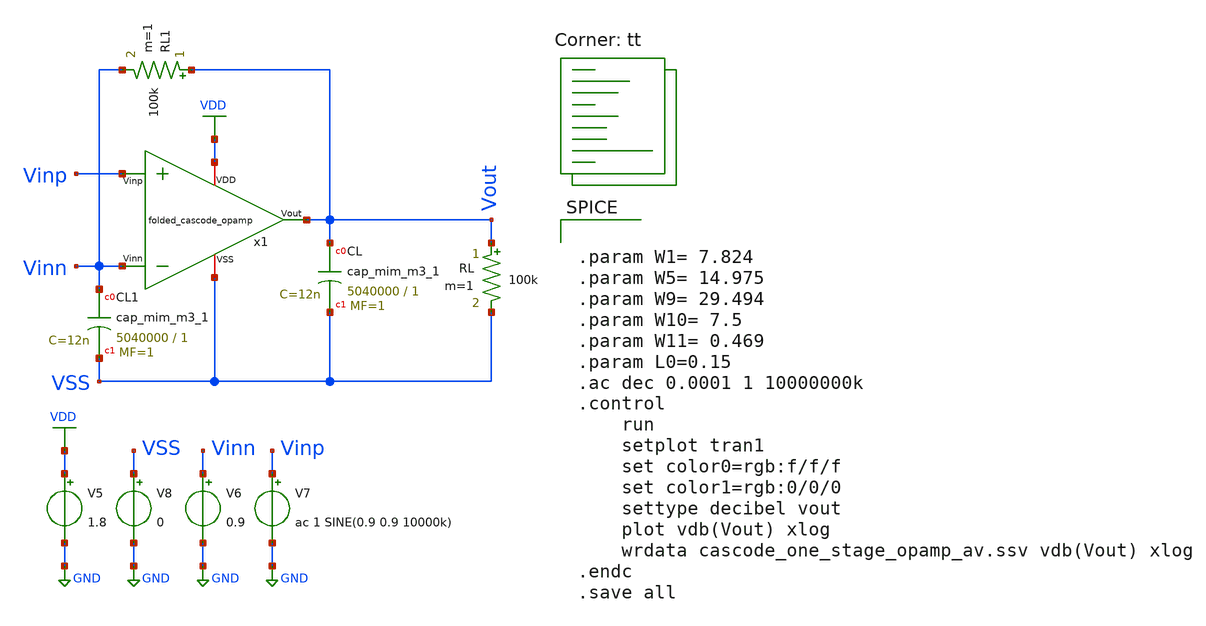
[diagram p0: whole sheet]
** sch_path: opamp_design/folded_cascode_opamp/folded_one_stage_opamp_av.sch
**.subckt folded_one_stage_opamp_av
XCL Vout VSS sky130_fd_pr__cap_mim_m3_1 W=5040000 L=1 MF=1 m=1
RL Vout VSS 100k m=1
XCL1 Vinn VSS sky130_fd_pr__cap_mim_m3_1 W=5040000 L=1 MF=1 m=1
RL1 Vout Vinn 100k m=1
V5 VDD GND 1.8
V6 Vinn GND 0.9
V7 Vinp GND ac 1 SINE(0.9 0.9 10000k)
V8 VSS GND 0
x1 VDD Vout Vinp Vinn VSS folded_cascode_opamp
**** begin user architecture code
.lib $::SKYWATER_MODELS/sky130.lib.spice tt


.param W1= 7.824
.param W5= 14.975
.param W9= 29.494
.param W10= 7.5
.param W11= 0.469
.param L0=0.15
.ac dec 0.0001 1 10000000k
.control
	run
	setplot tran1
	set color0=rgb:f/f/f
	set color1=rgb:0/0/0
	settype decibel vout
	plot vdb(Vout) xlog
	wrdata cascode_one_stage_opamp_av.ssv vdb(Vout) xlog
.endc
.save all


**** end user architecture code
**.ends

* expanding   symbol:
*+  /home/ricardo/RATT_repos/Proyectos_xschem/opamp_design/folded_cascode_opamp/folded_cascode_opamp.sym # of pins=5
** sym_path: opamp_design/folded_cascode_opamp/folded_cascode_opamp.sym
** sch_path: opamp_design/folded_cascode_opamp/folded_cascode_opamp.sch
.subckt folded_cascode_opamp VDD Vout Vinp Vinn VSS
*.opin Vout
*.ipin Vinn
*.ipin Vinp
*.iopin VDD
*.iopin VSS
XM11 net4 net2 VSS VSS sky130_fd_pr__nfet_01v8 L={L0} W={W8} nf=1 ad='int((nf+1)/2) * W/nf * 0.29' as='int((nf+2)/2) * W/nf * 0.29'
+ pd='2*int((nf+1)/2) * (W/nf + 0.29)' ps='2*int((nf+2)/2) * (W/nf + 0.29)' nrd='0.29 / W' nrs='0.29 / W'
+ sa=0 sb=0 sd=0 mult=1 m=1
XM10 net3 net2 VSS VSS sky130_fd_pr__nfet_01v8 L={L0} W={W8} nf=1 ad='int((nf+1)/2) * W/nf * 0.29' as='int((nf+2)/2) * W/nf * 0.29'
+ pd='2*int((nf+1)/2) * (W/nf + 0.29)' ps='2*int((nf+2)/2) * (W/nf + 0.29)' nrd='0.29 / W' nrs='0.29 / W'
+ sa=0 sb=0 sd=0 mult=1 m=1
XM8 net2 net1 net3 VSS sky130_fd_pr__nfet_01v8 L={L0} W={W8} nf=1 ad='int((nf+1)/2) * W/nf * 0.29' as='int((nf+2)/2) * W/nf * 0.29'
+ pd='2*int((nf+1)/2) * (W/nf + 0.29)' ps='2*int((nf+2)/2) * (W/nf + 0.29)' nrd='0.29 / W' nrs='0.29 / W'
+ sa=0 sb=0 sd=0 mult=1 m=1
XM9 Vout net1 net4 VSS sky130_fd_pr__nfet_01v8 L={L0} W={W8} nf=1 ad='int((nf+1)/2) * W/nf * 0.29' as='int((nf+2)/2) * W/nf * 0.29'
+ pd='2*int((nf+1)/2) * (W/nf + 0.29)' ps='2*int((nf+2)/2) * (W/nf + 0.29)' nrd='0.29 / W' nrs='0.29 / W'
+ sa=0 sb=0 sd=0 mult=1 m=1
XM7 Vout net5 net8 VDD sky130_fd_pr__pfet_01v8 L={L0} W={W6} nf=1 ad='int((nf+1)/2) * W/nf * 0.29' as='int((nf+2)/2) * W/nf * 0.29'
+ pd='2*int((nf+1)/2) * (W/nf + 0.29)' ps='2*int((nf+2)/2) * (W/nf + 0.29)' nrd='0.29 / W' nrs='0.29 / W'
+ sa=0 sb=0 sd=0 mult=1 m=1
XM6 net2 net5 net7 VDD sky130_fd_pr__pfet_01v8 L={L0} W={W6} nf=1 ad='int((nf+1)/2) * W/nf * 0.29' as='int((nf+2)/2) * W/nf * 0.29'
+ pd='2*int((nf+1)/2) * (W/nf + 0.29)' ps='2*int((nf+2)/2) * (W/nf + 0.29)' nrd='0.29 / W' nrs='0.29 / W'
+ sa=0 sb=0 sd=0 mult=1 m=1
XM1 net7 Vinp net6 VSS sky130_fd_pr__nfet_01v8 L={L0} W={W1} nf=1 ad='int((nf+1)/2) * W/nf * 0.29' as='int((nf+2)/2) * W/nf * 0.29'
+ pd='2*int((nf+1)/2) * (W/nf + 0.29)' ps='2*int((nf+2)/2) * (W/nf + 0.29)' nrd='0.29 / W' nrs='0.29 / W'
+ sa=0 sb=0 sd=0 mult=1 m=1
XM2 net8 Vinn net6 VSS sky130_fd_pr__nfet_01v8 L={L0} W={W1} nf=1 ad='int((nf+1)/2) * W/nf * 0.29' as='int((nf+2)/2) * W/nf * 0.29'
+ pd='2*int((nf+1)/2) * (W/nf + 0.29)' ps='2*int((nf+2)/2) * (W/nf + 0.29)' nrd='0.29 / W' nrs='0.29 / W'
+ sa=0 sb=0 sd=0 mult=1 m=1
XM3 net6 net10 VSS VSS sky130_fd_pr__nfet_01v8 L={L0} W={W3} nf=1 ad='int((nf+1)/2) * W/nf * 0.29' as='int((nf+2)/2) * W/nf * 0.29'
+ pd='2*int((nf+1)/2) * (W/nf + 0.29)' ps='2*int((nf+2)/2) * (W/nf + 0.29)' nrd='0.29 / W' nrs='0.29 / W'
+ sa=0 sb=0 sd=0 mult=1 m=1
XM4 net7 net9 VDD VDD sky130_fd_pr__pfet_01v8 L={L0} W={W4} nf=1 ad='int((nf+1)/2) * W/nf * 0.29' as='int((nf+2)/2) * W/nf * 0.29'
+ pd='2*int((nf+1)/2) * (W/nf + 0.29)' ps='2*int((nf+2)/2) * (W/nf + 0.29)' nrd='0.29 / W' nrs='0.29 / W'
+ sa=0 sb=0 sd=0 mult=1 m=1
XM5 net8 net9 VDD VDD sky130_fd_pr__pfet_01v8 L={L0} W={W4} nf=1 ad='int((nf+1)/2) * W/nf * 0.29' as='int((nf+2)/2) * W/nf * 0.29'
+ pd='2*int((nf+1)/2) * (W/nf + 0.29)' ps='2*int((nf+2)/2) * (W/nf + 0.29)' nrd='0.29 / W' nrs='0.29 / W'
+ sa=0 sb=0 sd=0 mult=1 m=1
XC1 Vout VSS sky130_fd_pr__cap_mim_m3_1 W=1 L=1 MF=1 m=1
XM12 net9 net9 VDD VDD sky130_fd_pr__pfet_01v8 L={L0} W={W4} nf=1 ad='int((nf+1)/2) * W/nf * 0.29' as='int((nf+2)/2) * W/nf * 0.29'
+ pd='2*int((nf+1)/2) * (W/nf + 0.29)' ps='2*int((nf+2)/2) * (W/nf + 0.29)' nrd='0.29 / W' nrs='0.29 / W'
+ sa=0 sb=0 sd=0 mult=1 m=1
I4 net9 VSS 10u
XM13 net5 net5 VDD VDD sky130_fd_pr__pfet_01v8 L={L0} W={W6} nf=1 ad='int((nf+1)/2) * W/nf * 0.29' as='int((nf+2)/2) * W/nf * 0.29'
+ pd='2*int((nf+1)/2) * (W/nf + 0.29)' ps='2*int((nf+2)/2) * (W/nf + 0.29)' nrd='0.29 / W' nrs='0.29 / W'
+ sa=0 sb=0 sd=0 mult=1 m=1
I1 net5 VSS 10u
XM14 net1 net1 VSS VSS sky130_fd_pr__nfet_01v8 L={L0} W={W8} nf=1 ad='int((nf+1)/2) * W/nf * 0.29' as='int((nf+2)/2) * W/nf * 0.29'
+ pd='2*int((nf+1)/2) * (W/nf + 0.29)' ps='2*int((nf+2)/2) * (W/nf + 0.29)' nrd='0.29 / W' nrs='0.29 / W'
+ sa=0 sb=0 sd=0 mult=1 m=1
I2 VDD net1 10u
XM15 net10 net10 VSS VSS sky130_fd_pr__nfet_01v8 L={L0} W={W3} nf=1 ad='int((nf+1)/2) * W/nf * 0.29'
+ as='int((nf+2)/2) * W/nf * 0.29' pd='2*int((nf+1)/2) * (W/nf + 0.29)' ps='2*int((nf+2)/2) * (W/nf + 0.29)'
+ nrd='0.29 / W' nrs='0.29 / W' sa=0 sb=0 sd=0 mult=1 m=1
I3 VDD net10 10u
.ends

.GLOBAL VDD
.GLOBAL GND
.end
